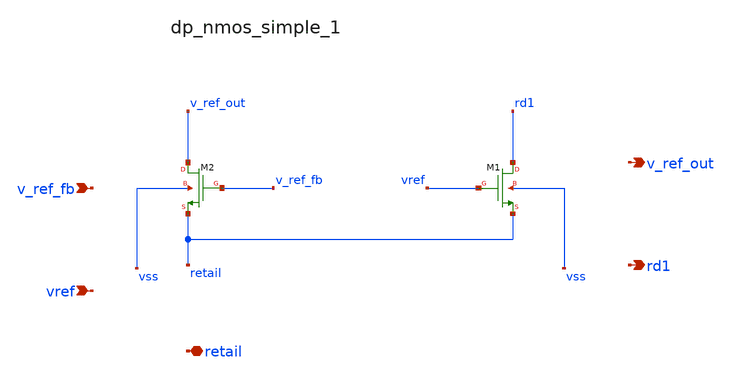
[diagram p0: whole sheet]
** sch_path: analog-db/raw/ldo_005_buffered_ref/hier/blocks/dp_nmos_simple_1.sch
**.subckt dp_nmos_simple_1 v_ref_fb vref retail v_ref_out rd1
*.ipin v_ref_fb
*.ipin vref
*.iopin retail
*.opin v_ref_out
*.opin rd1
XM1 rd1 vref retail vss sg13_lv_nmos w=x_dut_xm1_w l=x_dut_xm1_l ng=1 m=1
XM2 v_ref_out v_ref_fb retail vss sg13_lv_nmos w=x_dut_xm2_w l=x_dut_xm2_l ng=1 m=1
**.ends
.end
